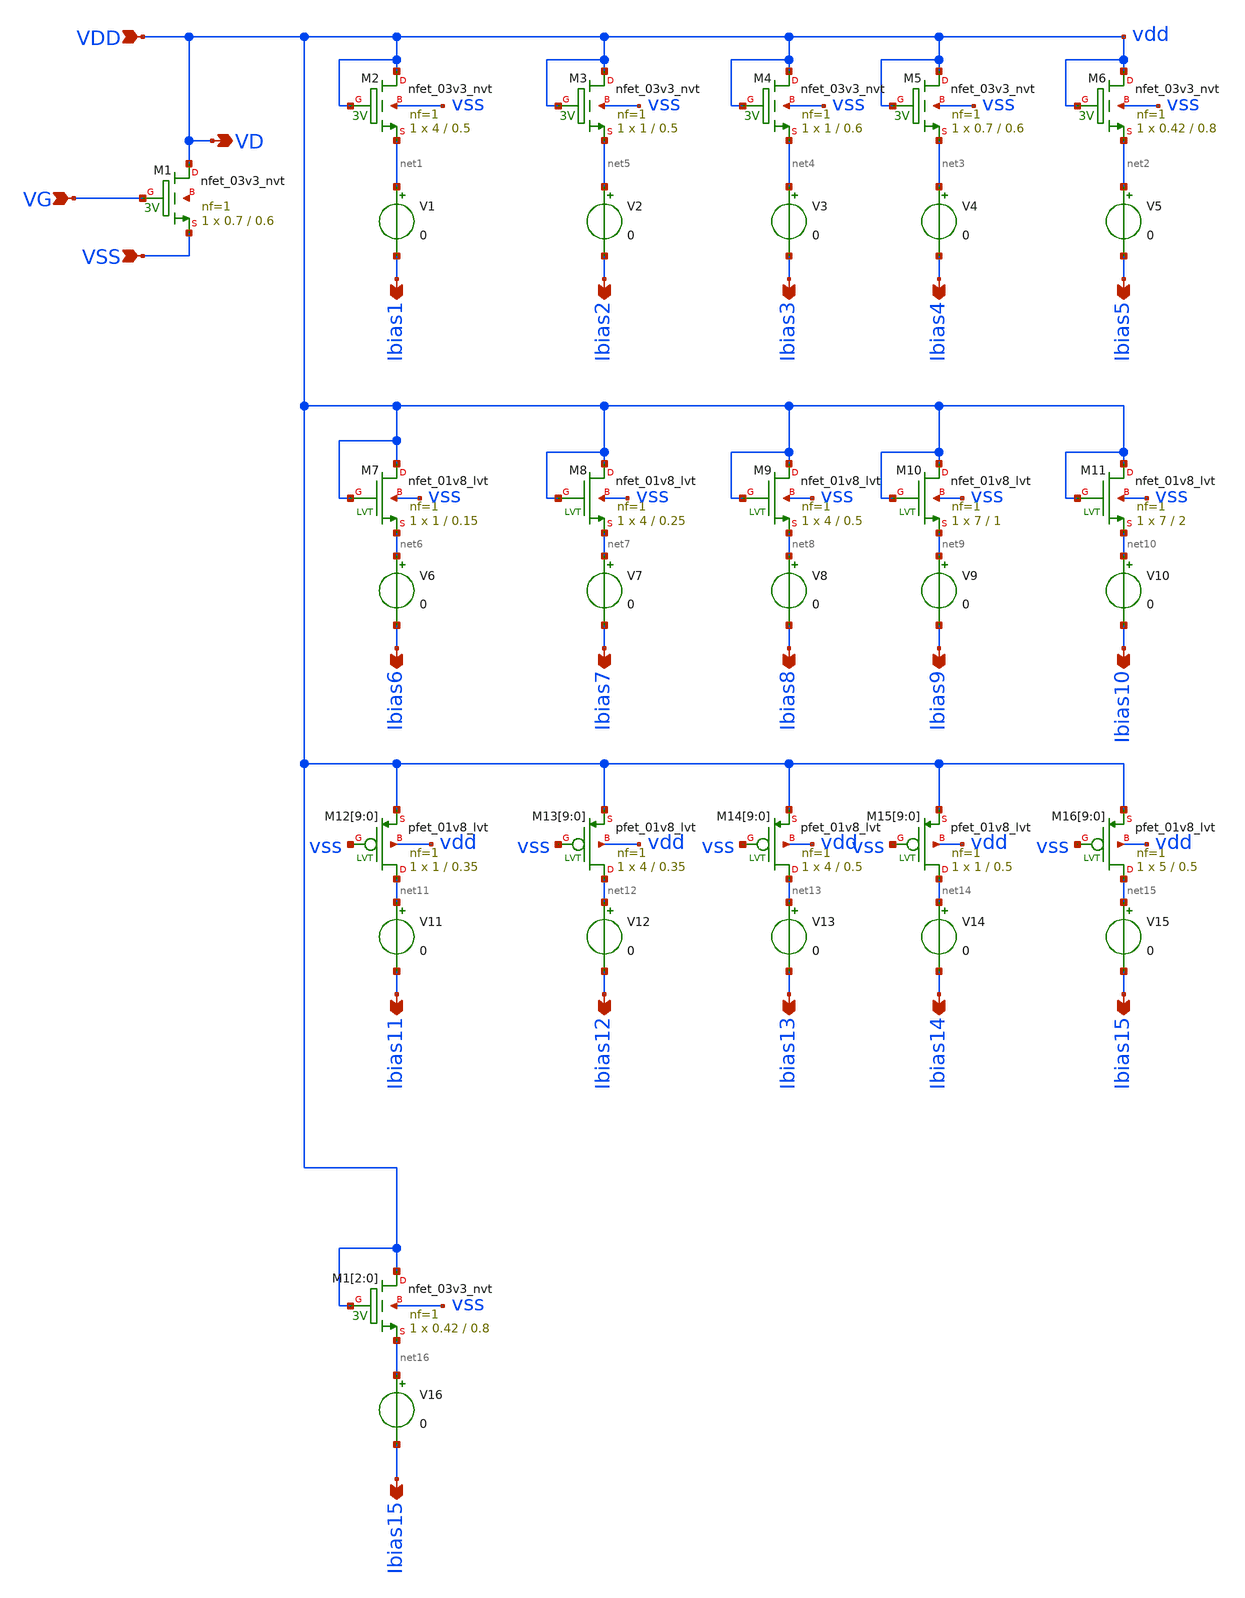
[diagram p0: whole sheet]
** sch_path: design/THESIS_EXP_RO_INVERTER_SKY130A/TB_FET_as_diode.sch
**.subckt TB_FET_as_diode VDD VSS VD VG Ibias1 Ibias2 Ibias3 Ibias4 Ibias5 Ibias6 Ibias7 Ibias8
*+ Ibias9 Ibias10 Ibias11 Ibias12 Ibias13 Ibias14 Ibias15 Ibias15
*.ipin VDD
*.ipin VSS
*.opin VD
*.ipin VG
*.opin Ibias1
*.opin Ibias2
*.opin Ibias3
*.opin Ibias4
*.opin Ibias5
*.opin Ibias6
*.opin Ibias7
*.opin Ibias8
*.opin Ibias9
*.opin Ibias10
*.opin Ibias11
*.opin Ibias12
*.opin Ibias13
*.opin Ibias14
*.opin Ibias15
*.opin Ibias15
XM1 VDD VG VSS net17 sky130_fd_pr__nfet_03v3_nvt L=0.6 W=0.7 nf=1 ad='int((nf+1)/2) * W/nf * 0.29' as='int((nf+2)/2) * W/nf * 0.29'
+ pd='2*int((nf+1)/2) * (W/nf + 0.29)' ps='2*int((nf+2)/2) * (W/nf + 0.29)' nrd='0.29 / W' nrs='0.29 / W'
+ sa=0 sb=0 sd=0 mult=1 m=1
XM2 VDD VDD net1 vss sky130_fd_pr__nfet_03v3_nvt L=0.5 W=4 nf=1 ad='int((nf+1)/2) * W/nf * 0.29' as='int((nf+2)/2) * W/nf * 0.29'
+ pd='2*int((nf+1)/2) * (W/nf + 0.29)' ps='2*int((nf+2)/2) * (W/nf + 0.29)' nrd='0.29 / W' nrs='0.29 / W'
+ sa=0 sb=0 sd=0 mult=1 m=1
V1 net1 Ibias1 0
.save i(v1)
XM3 VDD VDD net5 vss sky130_fd_pr__nfet_03v3_nvt L=0.5 W=1 nf=1 ad='int((nf+1)/2) * W/nf * 0.29' as='int((nf+2)/2) * W/nf * 0.29'
+ pd='2*int((nf+1)/2) * (W/nf + 0.29)' ps='2*int((nf+2)/2) * (W/nf + 0.29)' nrd='0.29 / W' nrs='0.29 / W'
+ sa=0 sb=0 sd=0 mult=1 m=1
XM4 VDD VDD net4 vss sky130_fd_pr__nfet_03v3_nvt L=0.6 W=1 nf=1 ad='int((nf+1)/2) * W/nf * 0.29' as='int((nf+2)/2) * W/nf * 0.29'
+ pd='2*int((nf+1)/2) * (W/nf + 0.29)' ps='2*int((nf+2)/2) * (W/nf + 0.29)' nrd='0.29 / W' nrs='0.29 / W'
+ sa=0 sb=0 sd=0 mult=1 m=1
XM5 VDD VDD net3 vss sky130_fd_pr__nfet_03v3_nvt L=0.6 W=0.7 nf=1 ad='int((nf+1)/2) * W/nf * 0.29' as='int((nf+2)/2) * W/nf * 0.29'
+ pd='2*int((nf+1)/2) * (W/nf + 0.29)' ps='2*int((nf+2)/2) * (W/nf + 0.29)' nrd='0.29 / W' nrs='0.29 / W'
+ sa=0 sb=0 sd=0 mult=1 m=1
V2 net5 Ibias2 0
.save i(v2)
V3 net4 Ibias3 0
.save i(v3)
V4 net3 Ibias4 0
.save i(v4)
XM6 VDD VDD net2 vss sky130_fd_pr__nfet_03v3_nvt L=0.8 W=0.42 nf=1 ad='int((nf+1)/2) * W/nf * 0.29' as='int((nf+2)/2) * W/nf * 0.29'
+ pd='2*int((nf+1)/2) * (W/nf + 0.29)' ps='2*int((nf+2)/2) * (W/nf + 0.29)' nrd='0.29 / W' nrs='0.29 / W'
+ sa=0 sb=0 sd=0 mult=1 m=1
V5 net2 Ibias5 0
.save i(v5)
V6 net6 Ibias6 0
.save i(v6)
V7 net7 Ibias7 0
.save i(v7)
V8 net8 Ibias8 0
.save i(v8)
V9 net9 Ibias9 0
.save i(v9)
V10 net10 Ibias10 0
.save i(v10)
XM7 VDD VDD net6 vss sky130_fd_pr__nfet_01v8_lvt L=0.15 W=1 nf=1 ad='int((nf+1)/2) * W/nf * 0.29' as='int((nf+2)/2) * W/nf * 0.29'
+ pd='2*int((nf+1)/2) * (W/nf + 0.29)' ps='2*int((nf+2)/2) * (W/nf + 0.29)' nrd='0.29 / W' nrs='0.29 / W'
+ sa=0 sb=0 sd=0 mult=1 m=1
XM8 VDD VDD net7 vss sky130_fd_pr__nfet_01v8_lvt L=0.25 W=4 nf=1 ad='int((nf+1)/2) * W/nf * 0.29' as='int((nf+2)/2) * W/nf * 0.29'
+ pd='2*int((nf+1)/2) * (W/nf + 0.29)' ps='2*int((nf+2)/2) * (W/nf + 0.29)' nrd='0.29 / W' nrs='0.29 / W'
+ sa=0 sb=0 sd=0 mult=1 m=1
XM9 VDD VDD net8 vss sky130_fd_pr__nfet_01v8_lvt L=0.5 W=4 nf=1 ad='int((nf+1)/2) * W/nf * 0.29' as='int((nf+2)/2) * W/nf * 0.29'
+ pd='2*int((nf+1)/2) * (W/nf + 0.29)' ps='2*int((nf+2)/2) * (W/nf + 0.29)' nrd='0.29 / W' nrs='0.29 / W'
+ sa=0 sb=0 sd=0 mult=1 m=1
XM10 VDD VDD net9 vss sky130_fd_pr__nfet_01v8_lvt L=1 W=7 nf=1 ad='int((nf+1)/2) * W/nf * 0.29' as='int((nf+2)/2) * W/nf * 0.29'
+ pd='2*int((nf+1)/2) * (W/nf + 0.29)' ps='2*int((nf+2)/2) * (W/nf + 0.29)' nrd='0.29 / W' nrs='0.29 / W'
+ sa=0 sb=0 sd=0 mult=1 m=1
XM11 VDD VDD net10 vss sky130_fd_pr__nfet_01v8_lvt L=2 W=7 nf=1 ad='int((nf+1)/2) * W/nf * 0.29' as='int((nf+2)/2) * W/nf * 0.29'
+ pd='2*int((nf+1)/2) * (W/nf + 0.29)' ps='2*int((nf+2)/2) * (W/nf + 0.29)' nrd='0.29 / W' nrs='0.29 / W'
+ sa=0 sb=0 sd=0 mult=1 m=1
XM12[9] net11 vss VDD vdd sky130_fd_pr__pfet_01v8_lvt L=0.35 W=1 nf=1 ad='int((nf+1)/2) * W/nf * 0.29'
+ as='int((nf+2)/2) * W/nf * 0.29' pd='2*int((nf+1)/2) * (W/nf + 0.29)' ps='2*int((nf+2)/2) * (W/nf + 0.29)'
+ nrd='0.29 / W' nrs='0.29 / W' sa=0 sb=0 sd=0 mult=1 m=1
XM12[8] net11 vss VDD vdd sky130_fd_pr__pfet_01v8_lvt L=0.35 W=1 nf=1 ad='int((nf+1)/2) * W/nf * 0.29'
+ as='int((nf+2)/2) * W/nf * 0.29' pd='2*int((nf+1)/2) * (W/nf + 0.29)' ps='2*int((nf+2)/2) * (W/nf + 0.29)'
+ nrd='0.29 / W' nrs='0.29 / W' sa=0 sb=0 sd=0 mult=1 m=1
XM12[7] net11 vss VDD vdd sky130_fd_pr__pfet_01v8_lvt L=0.35 W=1 nf=1 ad='int((nf+1)/2) * W/nf * 0.29'
+ as='int((nf+2)/2) * W/nf * 0.29' pd='2*int((nf+1)/2) * (W/nf + 0.29)' ps='2*int((nf+2)/2) * (W/nf + 0.29)'
+ nrd='0.29 / W' nrs='0.29 / W' sa=0 sb=0 sd=0 mult=1 m=1
XM12[6] net11 vss VDD vdd sky130_fd_pr__pfet_01v8_lvt L=0.35 W=1 nf=1 ad='int((nf+1)/2) * W/nf * 0.29'
+ as='int((nf+2)/2) * W/nf * 0.29' pd='2*int((nf+1)/2) * (W/nf + 0.29)' ps='2*int((nf+2)/2) * (W/nf + 0.29)'
+ nrd='0.29 / W' nrs='0.29 / W' sa=0 sb=0 sd=0 mult=1 m=1
XM12[5] net11 vss VDD vdd sky130_fd_pr__pfet_01v8_lvt L=0.35 W=1 nf=1 ad='int((nf+1)/2) * W/nf * 0.29'
+ as='int((nf+2)/2) * W/nf * 0.29' pd='2*int((nf+1)/2) * (W/nf + 0.29)' ps='2*int((nf+2)/2) * (W/nf + 0.29)'
+ nrd='0.29 / W' nrs='0.29 / W' sa=0 sb=0 sd=0 mult=1 m=1
XM12[4] net11 vss VDD vdd sky130_fd_pr__pfet_01v8_lvt L=0.35 W=1 nf=1 ad='int((nf+1)/2) * W/nf * 0.29'
+ as='int((nf+2)/2) * W/nf * 0.29' pd='2*int((nf+1)/2) * (W/nf + 0.29)' ps='2*int((nf+2)/2) * (W/nf + 0.29)'
+ nrd='0.29 / W' nrs='0.29 / W' sa=0 sb=0 sd=0 mult=1 m=1
XM12[3] net11 vss VDD vdd sky130_fd_pr__pfet_01v8_lvt L=0.35 W=1 nf=1 ad='int((nf+1)/2) * W/nf * 0.29'
+ as='int((nf+2)/2) * W/nf * 0.29' pd='2*int((nf+1)/2) * (W/nf + 0.29)' ps='2*int((nf+2)/2) * (W/nf + 0.29)'
+ nrd='0.29 / W' nrs='0.29 / W' sa=0 sb=0 sd=0 mult=1 m=1
XM12[2] net11 vss VDD vdd sky130_fd_pr__pfet_01v8_lvt L=0.35 W=1 nf=1 ad='int((nf+1)/2) * W/nf * 0.29'
+ as='int((nf+2)/2) * W/nf * 0.29' pd='2*int((nf+1)/2) * (W/nf + 0.29)' ps='2*int((nf+2)/2) * (W/nf + 0.29)'
+ nrd='0.29 / W' nrs='0.29 / W' sa=0 sb=0 sd=0 mult=1 m=1
XM12[1] net11 vss VDD vdd sky130_fd_pr__pfet_01v8_lvt L=0.35 W=1 nf=1 ad='int((nf+1)/2) * W/nf * 0.29'
+ as='int((nf+2)/2) * W/nf * 0.29' pd='2*int((nf+1)/2) * (W/nf + 0.29)' ps='2*int((nf+2)/2) * (W/nf + 0.29)'
+ nrd='0.29 / W' nrs='0.29 / W' sa=0 sb=0 sd=0 mult=1 m=1
XM12[0] net11 vss VDD vdd sky130_fd_pr__pfet_01v8_lvt L=0.35 W=1 nf=1 ad='int((nf+1)/2) * W/nf * 0.29'
+ as='int((nf+2)/2) * W/nf * 0.29' pd='2*int((nf+1)/2) * (W/nf + 0.29)' ps='2*int((nf+2)/2) * (W/nf + 0.29)'
+ nrd='0.29 / W' nrs='0.29 / W' sa=0 sb=0 sd=0 mult=1 m=1
XM13[9] net12 vss VDD vdd sky130_fd_pr__pfet_01v8_lvt L=0.35 W=4 nf=1 ad='int((nf+1)/2) * W/nf * 0.29'
+ as='int((nf+2)/2) * W/nf * 0.29' pd='2*int((nf+1)/2) * (W/nf + 0.29)' ps='2*int((nf+2)/2) * (W/nf + 0.29)'
+ nrd='0.29 / W' nrs='0.29 / W' sa=0 sb=0 sd=0 mult=1 m=1
XM13[8] net12 vss VDD vdd sky130_fd_pr__pfet_01v8_lvt L=0.35 W=4 nf=1 ad='int((nf+1)/2) * W/nf * 0.29'
+ as='int((nf+2)/2) * W/nf * 0.29' pd='2*int((nf+1)/2) * (W/nf + 0.29)' ps='2*int((nf+2)/2) * (W/nf + 0.29)'
+ nrd='0.29 / W' nrs='0.29 / W' sa=0 sb=0 sd=0 mult=1 m=1
XM13[7] net12 vss VDD vdd sky130_fd_pr__pfet_01v8_lvt L=0.35 W=4 nf=1 ad='int((nf+1)/2) * W/nf * 0.29'
+ as='int((nf+2)/2) * W/nf * 0.29' pd='2*int((nf+1)/2) * (W/nf + 0.29)' ps='2*int((nf+2)/2) * (W/nf + 0.29)'
+ nrd='0.29 / W' nrs='0.29 / W' sa=0 sb=0 sd=0 mult=1 m=1
XM13[6] net12 vss VDD vdd sky130_fd_pr__pfet_01v8_lvt L=0.35 W=4 nf=1 ad='int((nf+1)/2) * W/nf * 0.29'
+ as='int((nf+2)/2) * W/nf * 0.29' pd='2*int((nf+1)/2) * (W/nf + 0.29)' ps='2*int((nf+2)/2) * (W/nf + 0.29)'
+ nrd='0.29 / W' nrs='0.29 / W' sa=0 sb=0 sd=0 mult=1 m=1
XM13[5] net12 vss VDD vdd sky130_fd_pr__pfet_01v8_lvt L=0.35 W=4 nf=1 ad='int((nf+1)/2) * W/nf * 0.29'
+ as='int((nf+2)/2) * W/nf * 0.29' pd='2*int((nf+1)/2) * (W/nf + 0.29)' ps='2*int((nf+2)/2) * (W/nf + 0.29)'
+ nrd='0.29 / W' nrs='0.29 / W' sa=0 sb=0 sd=0 mult=1 m=1
XM13[4] net12 vss VDD vdd sky130_fd_pr__pfet_01v8_lvt L=0.35 W=4 nf=1 ad='int((nf+1)/2) * W/nf * 0.29'
+ as='int((nf+2)/2) * W/nf * 0.29' pd='2*int((nf+1)/2) * (W/nf + 0.29)' ps='2*int((nf+2)/2) * (W/nf + 0.29)'
+ nrd='0.29 / W' nrs='0.29 / W' sa=0 sb=0 sd=0 mult=1 m=1
XM13[3] net12 vss VDD vdd sky130_fd_pr__pfet_01v8_lvt L=0.35 W=4 nf=1 ad='int((nf+1)/2) * W/nf * 0.29'
+ as='int((nf+2)/2) * W/nf * 0.29' pd='2*int((nf+1)/2) * (W/nf + 0.29)' ps='2*int((nf+2)/2) * (W/nf + 0.29)'
+ nrd='0.29 / W' nrs='0.29 / W' sa=0 sb=0 sd=0 mult=1 m=1
XM13[2] net12 vss VDD vdd sky130_fd_pr__pfet_01v8_lvt L=0.35 W=4 nf=1 ad='int((nf+1)/2) * W/nf * 0.29'
+ as='int((nf+2)/2) * W/nf * 0.29' pd='2*int((nf+1)/2) * (W/nf + 0.29)' ps='2*int((nf+2)/2) * (W/nf + 0.29)'
+ nrd='0.29 / W' nrs='0.29 / W' sa=0 sb=0 sd=0 mult=1 m=1
XM13[1] net12 vss VDD vdd sky130_fd_pr__pfet_01v8_lvt L=0.35 W=4 nf=1 ad='int((nf+1)/2) * W/nf * 0.29'
+ as='int((nf+2)/2) * W/nf * 0.29' pd='2*int((nf+1)/2) * (W/nf + 0.29)' ps='2*int((nf+2)/2) * (W/nf + 0.29)'
+ nrd='0.29 / W' nrs='0.29 / W' sa=0 sb=0 sd=0 mult=1 m=1
XM13[0] net12 vss VDD vdd sky130_fd_pr__pfet_01v8_lvt L=0.35 W=4 nf=1 ad='int((nf+1)/2) * W/nf * 0.29'
+ as='int((nf+2)/2) * W/nf * 0.29' pd='2*int((nf+1)/2) * (W/nf + 0.29)' ps='2*int((nf+2)/2) * (W/nf + 0.29)'
+ nrd='0.29 / W' nrs='0.29 / W' sa=0 sb=0 sd=0 mult=1 m=1
XM14[9] net13 vss VDD vdd sky130_fd_pr__pfet_01v8_lvt L=0.5 W=4 nf=1 ad='int((nf+1)/2) * W/nf * 0.29'
+ as='int((nf+2)/2) * W/nf * 0.29' pd='2*int((nf+1)/2) * (W/nf + 0.29)' ps='2*int((nf+2)/2) * (W/nf + 0.29)'
+ nrd='0.29 / W' nrs='0.29 / W' sa=0 sb=0 sd=0 mult=1 m=1
XM14[8] net13 vss VDD vdd sky130_fd_pr__pfet_01v8_lvt L=0.5 W=4 nf=1 ad='int((nf+1)/2) * W/nf * 0.29'
+ as='int((nf+2)/2) * W/nf * 0.29' pd='2*int((nf+1)/2) * (W/nf + 0.29)' ps='2*int((nf+2)/2) * (W/nf + 0.29)'
+ nrd='0.29 / W' nrs='0.29 / W' sa=0 sb=0 sd=0 mult=1 m=1
XM14[7] net13 vss VDD vdd sky130_fd_pr__pfet_01v8_lvt L=0.5 W=4 nf=1 ad='int((nf+1)/2) * W/nf * 0.29'
+ as='int((nf+2)/2) * W/nf * 0.29' pd='2*int((nf+1)/2) * (W/nf + 0.29)' ps='2*int((nf+2)/2) * (W/nf + 0.29)'
+ nrd='0.29 / W' nrs='0.29 / W' sa=0 sb=0 sd=0 mult=1 m=1
XM14[6] net13 vss VDD vdd sky130_fd_pr__pfet_01v8_lvt L=0.5 W=4 nf=1 ad='int((nf+1)/2) * W/nf * 0.29'
+ as='int((nf+2)/2) * W/nf * 0.29' pd='2*int((nf+1)/2) * (W/nf + 0.29)' ps='2*int((nf+2)/2) * (W/nf + 0.29)'
+ nrd='0.29 / W' nrs='0.29 / W' sa=0 sb=0 sd=0 mult=1 m=1
XM14[5] net13 vss VDD vdd sky130_fd_pr__pfet_01v8_lvt L=0.5 W=4 nf=1 ad='int((nf+1)/2) * W/nf * 0.29'
+ as='int((nf+2)/2) * W/nf * 0.29' pd='2*int((nf+1)/2) * (W/nf + 0.29)' ps='2*int((nf+2)/2) * (W/nf + 0.29)'
+ nrd='0.29 / W' nrs='0.29 / W' sa=0 sb=0 sd=0 mult=1 m=1
XM14[4] net13 vss VDD vdd sky130_fd_pr__pfet_01v8_lvt L=0.5 W=4 nf=1 ad='int((nf+1)/2) * W/nf * 0.29'
+ as='int((nf+2)/2) * W/nf * 0.29' pd='2*int((nf+1)/2) * (W/nf + 0.29)' ps='2*int((nf+2)/2) * (W/nf + 0.29)'
+ nrd='0.29 / W' nrs='0.29 / W' sa=0 sb=0 sd=0 mult=1 m=1
XM14[3] net13 vss VDD vdd sky130_fd_pr__pfet_01v8_lvt L=0.5 W=4 nf=1 ad='int((nf+1)/2) * W/nf * 0.29'
+ as='int((nf+2)/2) * W/nf * 0.29' pd='2*int((nf+1)/2) * (W/nf + 0.29)' ps='2*int((nf+2)/2) * (W/nf + 0.29)'
+ nrd='0.29 / W' nrs='0.29 / W' sa=0 sb=0 sd=0 mult=1 m=1
XM14[2] net13 vss VDD vdd sky130_fd_pr__pfet_01v8_lvt L=0.5 W=4 nf=1 ad='int((nf+1)/2) * W/nf * 0.29'
+ as='int((nf+2)/2) * W/nf * 0.29' pd='2*int((nf+1)/2) * (W/nf + 0.29)' ps='2*int((nf+2)/2) * (W/nf + 0.29)'
+ nrd='0.29 / W' nrs='0.29 / W' sa=0 sb=0 sd=0 mult=1 m=1
XM14[1] net13 vss VDD vdd sky130_fd_pr__pfet_01v8_lvt L=0.5 W=4 nf=1 ad='int((nf+1)/2) * W/nf * 0.29'
+ as='int((nf+2)/2) * W/nf * 0.29' pd='2*int((nf+1)/2) * (W/nf + 0.29)' ps='2*int((nf+2)/2) * (W/nf + 0.29)'
+ nrd='0.29 / W' nrs='0.29 / W' sa=0 sb=0 sd=0 mult=1 m=1
XM14[0] net13 vss VDD vdd sky130_fd_pr__pfet_01v8_lvt L=0.5 W=4 nf=1 ad='int((nf+1)/2) * W/nf * 0.29'
+ as='int((nf+2)/2) * W/nf * 0.29' pd='2*int((nf+1)/2) * (W/nf + 0.29)' ps='2*int((nf+2)/2) * (W/nf + 0.29)'
+ nrd='0.29 / W' nrs='0.29 / W' sa=0 sb=0 sd=0 mult=1 m=1
XM15[9] net14 vss VDD vdd sky130_fd_pr__pfet_01v8_lvt L=0.5 W=1 nf=1 ad='int((nf+1)/2) * W/nf * 0.29'
+ as='int((nf+2)/2) * W/nf * 0.29' pd='2*int((nf+1)/2) * (W/nf + 0.29)' ps='2*int((nf+2)/2) * (W/nf + 0.29)'
+ nrd='0.29 / W' nrs='0.29 / W' sa=0 sb=0 sd=0 mult=1 m=1
XM15[8] net14 vss VDD vdd sky130_fd_pr__pfet_01v8_lvt L=0.5 W=1 nf=1 ad='int((nf+1)/2) * W/nf * 0.29'
+ as='int((nf+2)/2) * W/nf * 0.29' pd='2*int((nf+1)/2) * (W/nf + 0.29)' ps='2*int((nf+2)/2) * (W/nf + 0.29)'
+ nrd='0.29 / W' nrs='0.29 / W' sa=0 sb=0 sd=0 mult=1 m=1
XM15[7] net14 vss VDD vdd sky130_fd_pr__pfet_01v8_lvt L=0.5 W=1 nf=1 ad='int((nf+1)/2) * W/nf * 0.29'
+ as='int((nf+2)/2) * W/nf * 0.29' pd='2*int((nf+1)/2) * (W/nf + 0.29)' ps='2*int((nf+2)/2) * (W/nf + 0.29)'
+ nrd='0.29 / W' nrs='0.29 / W' sa=0 sb=0 sd=0 mult=1 m=1
XM15[6] net14 vss VDD vdd sky130_fd_pr__pfet_01v8_lvt L=0.5 W=1 nf=1 ad='int((nf+1)/2) * W/nf * 0.29'
+ as='int((nf+2)/2) * W/nf * 0.29' pd='2*int((nf+1)/2) * (W/nf + 0.29)' ps='2*int((nf+2)/2) * (W/nf + 0.29)'
+ nrd='0.29 / W' nrs='0.29 / W' sa=0 sb=0 sd=0 mult=1 m=1
XM15[5] net14 vss VDD vdd sky130_fd_pr__pfet_01v8_lvt L=0.5 W=1 nf=1 ad='int((nf+1)/2) * W/nf * 0.29'
+ as='int((nf+2)/2) * W/nf * 0.29' pd='2*int((nf+1)/2) * (W/nf + 0.29)' ps='2*int((nf+2)/2) * (W/nf + 0.29)'
+ nrd='0.29 / W' nrs='0.29 / W' sa=0 sb=0 sd=0 mult=1 m=1
XM15[4] net14 vss VDD vdd sky130_fd_pr__pfet_01v8_lvt L=0.5 W=1 nf=1 ad='int((nf+1)/2) * W/nf * 0.29'
+ as='int((nf+2)/2) * W/nf * 0.29' pd='2*int((nf+1)/2) * (W/nf + 0.29)' ps='2*int((nf+2)/2) * (W/nf + 0.29)'
+ nrd='0.29 / W' nrs='0.29 / W' sa=0 sb=0 sd=0 mult=1 m=1
XM15[3] net14 vss VDD vdd sky130_fd_pr__pfet_01v8_lvt L=0.5 W=1 nf=1 ad='int((nf+1)/2) * W/nf * 0.29'
+ as='int((nf+2)/2) * W/nf * 0.29' pd='2*int((nf+1)/2) * (W/nf + 0.29)' ps='2*int((nf+2)/2) * (W/nf + 0.29)'
+ nrd='0.29 / W' nrs='0.29 / W' sa=0 sb=0 sd=0 mult=1 m=1
XM15[2] net14 vss VDD vdd sky130_fd_pr__pfet_01v8_lvt L=0.5 W=1 nf=1 ad='int((nf+1)/2) * W/nf * 0.29'
+ as='int((nf+2)/2) * W/nf * 0.29' pd='2*int((nf+1)/2) * (W/nf + 0.29)' ps='2*int((nf+2)/2) * (W/nf + 0.29)'
+ nrd='0.29 / W' nrs='0.29 / W' sa=0 sb=0 sd=0 mult=1 m=1
XM15[1] net14 vss VDD vdd sky130_fd_pr__pfet_01v8_lvt L=0.5 W=1 nf=1 ad='int((nf+1)/2) * W/nf * 0.29'
+ as='int((nf+2)/2) * W/nf * 0.29' pd='2*int((nf+1)/2) * (W/nf + 0.29)' ps='2*int((nf+2)/2) * (W/nf + 0.29)'
+ nrd='0.29 / W' nrs='0.29 / W' sa=0 sb=0 sd=0 mult=1 m=1
XM15[0] net14 vss VDD vdd sky130_fd_pr__pfet_01v8_lvt L=0.5 W=1 nf=1 ad='int((nf+1)/2) * W/nf * 0.29'
+ as='int((nf+2)/2) * W/nf * 0.29' pd='2*int((nf+1)/2) * (W/nf + 0.29)' ps='2*int((nf+2)/2) * (W/nf + 0.29)'
+ nrd='0.29 / W' nrs='0.29 / W' sa=0 sb=0 sd=0 mult=1 m=1
XM16[9] net15 vss VDD vdd sky130_fd_pr__pfet_01v8_lvt L=0.5 W=5 nf=1 ad='int((nf+1)/2) * W/nf * 0.29'
+ as='int((nf+2)/2) * W/nf * 0.29' pd='2*int((nf+1)/2) * (W/nf + 0.29)' ps='2*int((nf+2)/2) * (W/nf + 0.29)'
+ nrd='0.29 / W' nrs='0.29 / W' sa=0 sb=0 sd=0 mult=1 m=1
XM16[8] net15 vss VDD vdd sky130_fd_pr__pfet_01v8_lvt L=0.5 W=5 nf=1 ad='int((nf+1)/2) * W/nf * 0.29'
+ as='int((nf+2)/2) * W/nf * 0.29' pd='2*int((nf+1)/2) * (W/nf + 0.29)' ps='2*int((nf+2)/2) * (W/nf + 0.29)'
+ nrd='0.29 / W' nrs='0.29 / W' sa=0 sb=0 sd=0 mult=1 m=1
XM16[7] net15 vss VDD vdd sky130_fd_pr__pfet_01v8_lvt L=0.5 W=5 nf=1 ad='int((nf+1)/2) * W/nf * 0.29'
+ as='int((nf+2)/2) * W/nf * 0.29' pd='2*int((nf+1)/2) * (W/nf + 0.29)' ps='2*int((nf+2)/2) * (W/nf + 0.29)'
+ nrd='0.29 / W' nrs='0.29 / W' sa=0 sb=0 sd=0 mult=1 m=1
XM16[6] net15 vss VDD vdd sky130_fd_pr__pfet_01v8_lvt L=0.5 W=5 nf=1 ad='int((nf+1)/2) * W/nf * 0.29'
+ as='int((nf+2)/2) * W/nf * 0.29' pd='2*int((nf+1)/2) * (W/nf + 0.29)' ps='2*int((nf+2)/2) * (W/nf + 0.29)'
+ nrd='0.29 / W' nrs='0.29 / W' sa=0 sb=0 sd=0 mult=1 m=1
XM16[5] net15 vss VDD vdd sky130_fd_pr__pfet_01v8_lvt L=0.5 W=5 nf=1 ad='int((nf+1)/2) * W/nf * 0.29'
+ as='int((nf+2)/2) * W/nf * 0.29' pd='2*int((nf+1)/2) * (W/nf + 0.29)' ps='2*int((nf+2)/2) * (W/nf + 0.29)'
+ nrd='0.29 / W' nrs='0.29 / W' sa=0 sb=0 sd=0 mult=1 m=1
XM16[4] net15 vss VDD vdd sky130_fd_pr__pfet_01v8_lvt L=0.5 W=5 nf=1 ad='int((nf+1)/2) * W/nf * 0.29'
+ as='int((nf+2)/2) * W/nf * 0.29' pd='2*int((nf+1)/2) * (W/nf + 0.29)' ps='2*int((nf+2)/2) * (W/nf + 0.29)'
+ nrd='0.29 / W' nrs='0.29 / W' sa=0 sb=0 sd=0 mult=1 m=1
XM16[3] net15 vss VDD vdd sky130_fd_pr__pfet_01v8_lvt L=0.5 W=5 nf=1 ad='int((nf+1)/2) * W/nf * 0.29'
+ as='int((nf+2)/2) * W/nf * 0.29' pd='2*int((nf+1)/2) * (W/nf + 0.29)' ps='2*int((nf+2)/2) * (W/nf + 0.29)'
+ nrd='0.29 / W' nrs='0.29 / W' sa=0 sb=0 sd=0 mult=1 m=1
XM16[2] net15 vss VDD vdd sky130_fd_pr__pfet_01v8_lvt L=0.5 W=5 nf=1 ad='int((nf+1)/2) * W/nf * 0.29'
+ as='int((nf+2)/2) * W/nf * 0.29' pd='2*int((nf+1)/2) * (W/nf + 0.29)' ps='2*int((nf+2)/2) * (W/nf + 0.29)'
+ nrd='0.29 / W' nrs='0.29 / W' sa=0 sb=0 sd=0 mult=1 m=1
XM16[1] net15 vss VDD vdd sky130_fd_pr__pfet_01v8_lvt L=0.5 W=5 nf=1 ad='int((nf+1)/2) * W/nf * 0.29'
+ as='int((nf+2)/2) * W/nf * 0.29' pd='2*int((nf+1)/2) * (W/nf + 0.29)' ps='2*int((nf+2)/2) * (W/nf + 0.29)'
+ nrd='0.29 / W' nrs='0.29 / W' sa=0 sb=0 sd=0 mult=1 m=1
XM16[0] net15 vss VDD vdd sky130_fd_pr__pfet_01v8_lvt L=0.5 W=5 nf=1 ad='int((nf+1)/2) * W/nf * 0.29'
+ as='int((nf+2)/2) * W/nf * 0.29' pd='2*int((nf+1)/2) * (W/nf + 0.29)' ps='2*int((nf+2)/2) * (W/nf + 0.29)'
+ nrd='0.29 / W' nrs='0.29 / W' sa=0 sb=0 sd=0 mult=1 m=1
V11 net11 Ibias11 0
.save i(v11)
V12 net12 Ibias12 0
.save i(v12)
V13 net13 Ibias13 0
.save i(v13)
V14 net14 Ibias14 0
.save i(v14)
V15 net15 Ibias15 0
.save i(v15)
XM1[2] VDD VDD net16 vss sky130_fd_pr__nfet_03v3_nvt L=0.8 W=0.42 nf=1 ad='int((nf+1)/2) * W/nf * 0.29'
+ as='int((nf+2)/2) * W/nf * 0.29' pd='2*int((nf+1)/2) * (W/nf + 0.29)' ps='2*int((nf+2)/2) * (W/nf + 0.29)'
+ nrd='0.29 / W' nrs='0.29 / W' sa=0 sb=0 sd=0 mult=1 m=1
XM1[1] VDD VDD net16 vss sky130_fd_pr__nfet_03v3_nvt L=0.8 W=0.42 nf=1 ad='int((nf+1)/2) * W/nf * 0.29'
+ as='int((nf+2)/2) * W/nf * 0.29' pd='2*int((nf+1)/2) * (W/nf + 0.29)' ps='2*int((nf+2)/2) * (W/nf + 0.29)'
+ nrd='0.29 / W' nrs='0.29 / W' sa=0 sb=0 sd=0 mult=1 m=1
XM1[0] VDD VDD net16 vss sky130_fd_pr__nfet_03v3_nvt L=0.8 W=0.42 nf=1 ad='int((nf+1)/2) * W/nf * 0.29'
+ as='int((nf+2)/2) * W/nf * 0.29' pd='2*int((nf+1)/2) * (W/nf + 0.29)' ps='2*int((nf+2)/2) * (W/nf + 0.29)'
+ nrd='0.29 / W' nrs='0.29 / W' sa=0 sb=0 sd=0 mult=1 m=1
V16 net16 Ibias15 0
.save i(v16)
**.ends
.end
